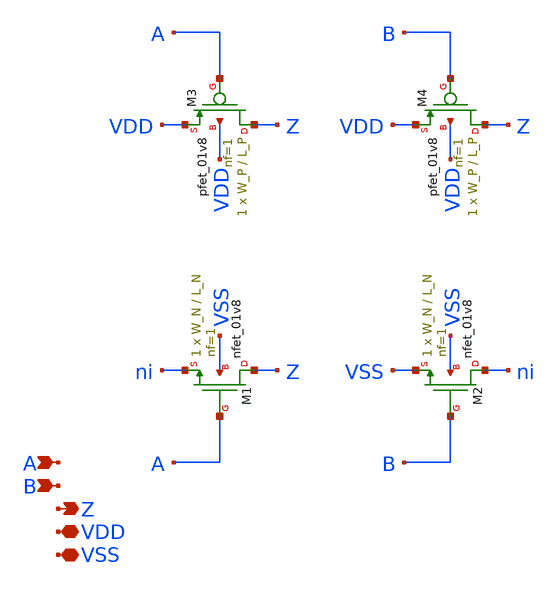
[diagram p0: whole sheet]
** sch_path: pipeline/analog/nand2/nand2.sch
**.subckt nand2 A B Z VDD VSS
*.ipin A
*.ipin B
*.opin Z
*.iopin VDD
*.iopin VSS
XM1 Z A ni VSS sky130_fd_pr__nfet_01v8 L=L_N W=W_N nf=1 ad='int((nf+1)/2) * W/nf * 0.29' as='int((nf+2)/2) * W/nf * 0.29'
+ pd='2*int((nf+1)/2) * (W/nf + 0.29)' ps='2*int((nf+2)/2) * (W/nf + 0.29)' nrd='0.29 / W' nrs='0.29 / W'
+ sa=0 sb=0 sd=0 mult=1 m=1
XM2 ni B VSS VSS sky130_fd_pr__nfet_01v8 L=L_N W=W_N nf=1 ad='int((nf+1)/2) * W/nf * 0.29' as='int((nf+2)/2) * W/nf * 0.29'
+ pd='2*int((nf+1)/2) * (W/nf + 0.29)' ps='2*int((nf+2)/2) * (W/nf + 0.29)' nrd='0.29 / W' nrs='0.29 / W'
+ sa=0 sb=0 sd=0 mult=1 m=1
XM3 Z A VDD VDD sky130_fd_pr__pfet_01v8 L=L_P W=W_P nf=1 ad='int((nf+1)/2) * W/nf * 0.29' as='int((nf+2)/2) * W/nf * 0.29'
+ pd='2*int((nf+1)/2) * (W/nf + 0.29)' ps='2*int((nf+2)/2) * (W/nf + 0.29)' nrd='0.29 / W' nrs='0.29 / W'
+ sa=0 sb=0 sd=0 mult=1 m=1
XM4 Z B VDD VDD sky130_fd_pr__pfet_01v8 L=L_P W=W_P nf=1 ad='int((nf+1)/2) * W/nf * 0.29' as='int((nf+2)/2) * W/nf * 0.29'
+ pd='2*int((nf+1)/2) * (W/nf + 0.29)' ps='2*int((nf+2)/2) * (W/nf + 0.29)' nrd='0.29 / W' nrs='0.29 / W'
+ sa=0 sb=0 sd=0 mult=1 m=1
**.ends
.end
